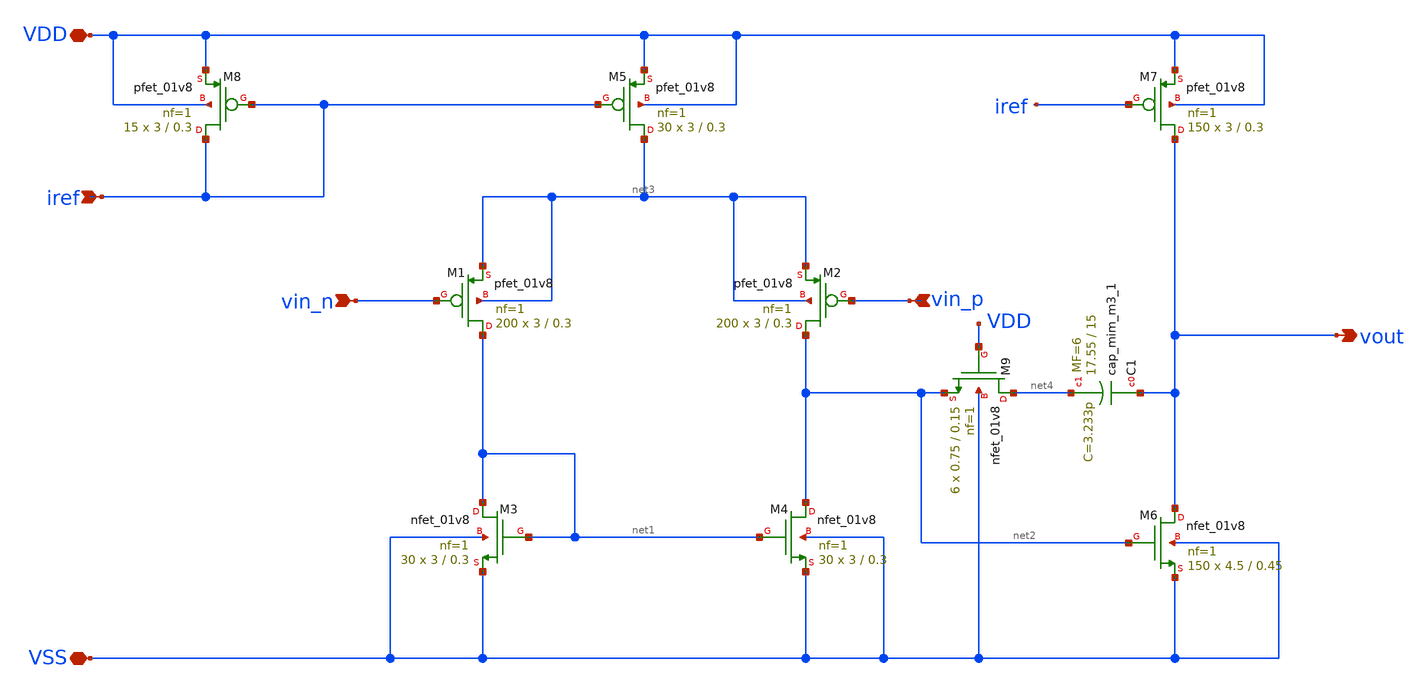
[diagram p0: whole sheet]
** sch_path: xschem/opamp_diego/opamp_v1.sch
**.subckt opamp_v1 VDD VSS iref vout vin_n vin_p
*.iopin VDD
*.iopin VSS
*.ipin iref
*.opin vout
*.ipin vin_n
*.ipin vin_p
XM1 net1 vin_n net3 net3 sky130_fd_pr__pfet_01v8 L=0.3 W=3 nf=1 ad='W * 0.29' as='W * 0.29' pd='2 * (W + 0.29)'
+ ps='2 * (W + 0.29)' nrd='0.29 / W' nrs='0.29 / W' sa=0 sb=0 sd=0 mult=200 m=200
XM2 net2 vin_p net3 net3 sky130_fd_pr__pfet_01v8 L=0.3 W=3 nf=1 ad='W * 0.29' as='W * 0.29' pd='2 * (W + 0.29)'
+ ps='2 * (W + 0.29)' nrd='0.29 / W' nrs='0.29 / W' sa=0 sb=0 sd=0 mult=200 m=200
XM3 net1 net1 VSS VSS sky130_fd_pr__nfet_01v8 L=0.3 W=3 nf=1 ad='W * 0.29' as='W * 0.29' pd='2 * (W + 0.29)'
+ ps='2 * (W + 0.29)' nrd='0.29 / W' nrs='0.29 / W' sa=0 sb=0 sd=0 mult=30 m=30
XM4 net2 net1 VSS VSS sky130_fd_pr__nfet_01v8 L=0.3 W=3 nf=1 ad='W * 0.29' as='W * 0.29' pd='2 * (W + 0.29)'
+ ps='2 * (W + 0.29)' nrd='0.29 / W' nrs='0.29 / W' sa=0 sb=0 sd=0 mult=30 m=30
XM5 net3 iref VDD VDD sky130_fd_pr__pfet_01v8 L=0.3 W=3 nf=1 ad='W * 0.29' as='W * 0.29' pd='2 * (W + 0.29)'
+ ps='2 * (W + 0.29)' nrd='0.29 / W' nrs='0.29 / W' sa=0 sb=0 sd=0 mult=30 m=30
XM7 vout iref VDD VDD sky130_fd_pr__pfet_01v8 L=0.3 W=3 nf=1 ad='W * 0.29' as='W * 0.29' pd='2 * (W + 0.29)'
+ ps='2 * (W + 0.29)' nrd='0.29 / W' nrs='0.29 / W' sa=0 sb=0 sd=0 mult=150 m=150
XM8 iref iref VDD VDD sky130_fd_pr__pfet_01v8 L=0.3 W=3 nf=1 ad='W * 0.29' as='W * 0.29' pd='2 * (W + 0.29)'
+ ps='2 * (W + 0.29)' nrd='0.29 / W' nrs='0.29 / W' sa=0 sb=0 sd=0 mult=15 m=15
XM9 net4 VDD net2 VSS sky130_fd_pr__nfet_01v8 L=0.15 W=0.75 nf=1 ad='W * 0.29' as='W * 0.29' pd='2 * (W + 0.29)'
+ ps='2 * (W + 0.29)' nrd='0.29 / W' nrs='0.29 / W' sa=0 sb=0 sd=0 mult=6 m=6
XC1 vout net4 sky130_fd_pr__cap_mim_m3_1 W=17.55 L=15 MF=6 m=6
XM6 vout net2 VSS VSS sky130_fd_pr__nfet_01v8 L=0.45 W=4.5 nf=1 ad='W * 0.29' as='W * 0.29' pd='2 * (W + 0.29)'
+ ps='2 * (W + 0.29)' nrd='0.29 / W' nrs='0.29 / W' sa=0 sb=0 sd=0 mult=150 m=150
**.ends
.end
